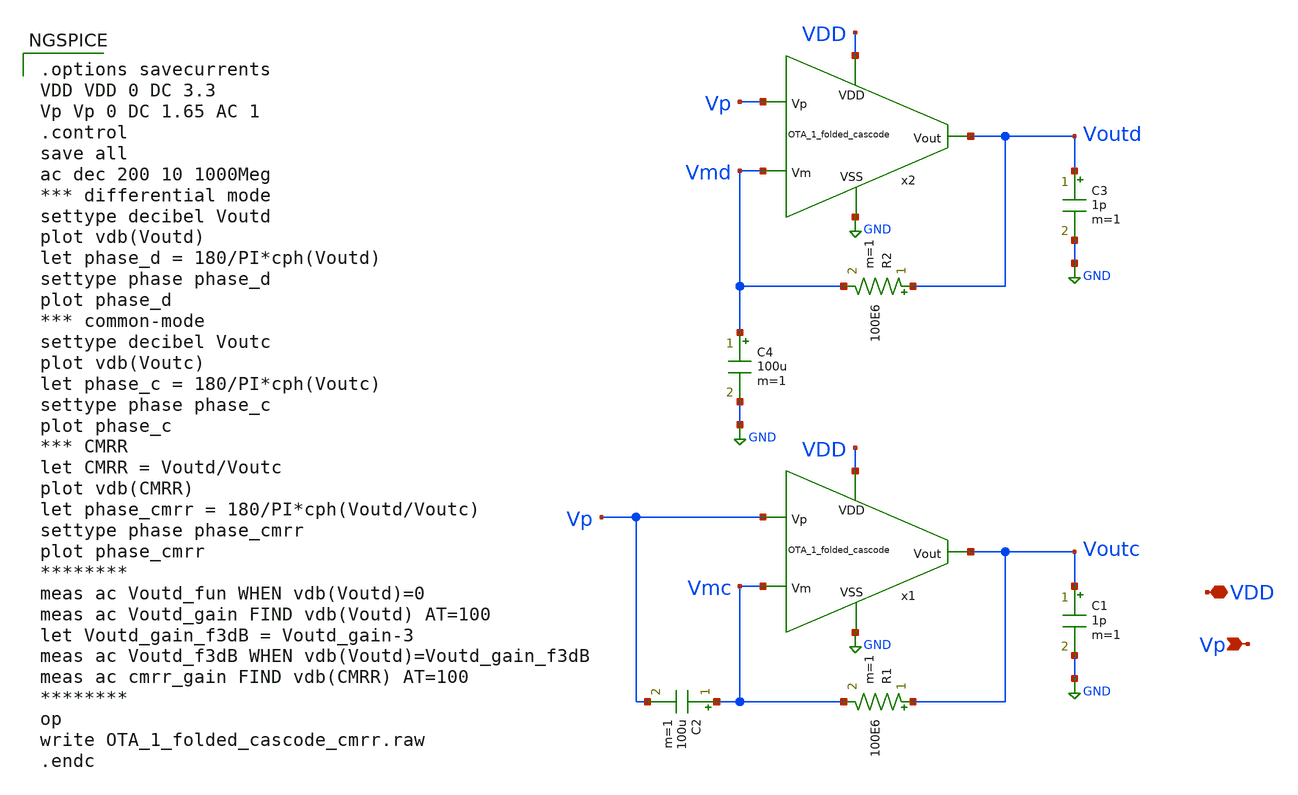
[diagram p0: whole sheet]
** sch_path: xschem/OTA_1_folded_cascode_cmrr.sch
**.subckt OTA_1_folded_cascode_cmrr VDD Vp
*.iopin VDD
*.ipin Vp
C1 Voutc GND 1p m=1
R1 Voutc Vmc 100E6 m=1
C2 Vmc Vp 100u m=1
x1 VDD Vp GND Vmc Voutc OTA_1_folded_cascode
C3 Voutd GND 1p m=1
R2 Voutd Vmd 100E6 m=1
C4 Vmd GND 100u m=1
x2 VDD Vp GND Vmd Voutd OTA_1_folded_cascode
**** begin user architecture code

.options savecurrents
VDD VDD 0 DC 3.3
Vp Vp 0 DC 1.65 AC 1
.control
save all
ac dec 200 10 1000Meg
*** differential mode
settype decibel Voutd
plot vdb(Voutd)
let phase_d = 180/PI*cph(Voutd)
settype phase phase_d
plot phase_d
*** common-mode
settype decibel Voutc
plot vdb(Voutc)
let phase_c = 180/PI*cph(Voutc)
settype phase phase_c
plot phase_c
*** CMRR
let CMRR = Voutd/Voutc
plot vdb(CMRR)
let phase_cmrr = 180/PI*cph(Voutd/Voutc)
settype phase phase_cmrr
plot phase_cmrr
********
meas ac Voutd_fun WHEN vdb(Voutd)=0
meas ac Voutd_gain FIND vdb(Voutd) AT=100
let Voutd_gain_f3dB = Voutd_gain-3
meas ac Voutd_f3dB WHEN vdb(Voutd)=Voutd_gain_f3dB
meas ac cmrr_gain FIND vdb(CMRR) AT=100
********
op
write OTA_1_folded_cascode_cmrr.raw
.endc



** opencircuitdesign pdks install
.lib $::SKYWATER_MODELS/sky130.lib.spice tt


**** end user architecture code
**.ends

* expanding   symbol:  OTA_1_folded_cascode.sym # of pins=5
** sym_path: xschem/OTA_1_folded_cascode.sym
** sch_path: xschem/OTA_1_folded_cascode.sch
.subckt OTA_1_folded_cascode VDD Vp VSS Vm Vout
*.iopin VDD
*.iopin VSS
*.ipin Vp
*.ipin Vm
*.opin Vout
XM1 Vo1 Vtop VDD VDD sky130_fd_pr__pfet_g5v0d10v5 L=1 W=5 nf=1 ad='int((nf+1)/2) * W/nf * 0.29' as='int((nf+2)/2) * W/nf * 0.29'
+ pd='2*int((nf+1)/2) * (W/nf + 0.29)' ps='2*int((nf+2)/2) * (W/nf + 0.29)' nrd='0.29 / W' nrs='0.29 / W'
+ sa=0 sb=0 sd=0 mult=5 m=5
XM7 Vo1 Vp net1 VSS sky130_fd_pr__nfet_g5v0d10v5 L=1 W=5 nf=1 ad='int((nf+1)/2) * W/nf * 0.29' as='int((nf+2)/2) * W/nf * 0.29'
+ pd='2*int((nf+1)/2) * (W/nf + 0.29)' ps='2*int((nf+2)/2) * (W/nf + 0.29)' nrd='0.29 / W' nrs='0.29 / W'
+ sa=0 sb=0 sd=0 mult=5 m=5
XM2 Vo1 Vtop VDD VDD sky130_fd_pr__pfet_g5v0d10v5 L=1 W=5 nf=1 ad='int((nf+1)/2) * W/nf * 0.29' as='int((nf+2)/2) * W/nf * 0.29'
+ pd='2*int((nf+1)/2) * (W/nf + 0.29)' ps='2*int((nf+2)/2) * (W/nf + 0.29)' nrd='0.29 / W' nrs='0.29 / W'
+ sa=0 sb=0 sd=0 mult=5 m=5
XM3 Vo2 Vtop VDD VDD sky130_fd_pr__pfet_g5v0d10v5 L=1 W=5 nf=1 ad='int((nf+1)/2) * W/nf * 0.29' as='int((nf+2)/2) * W/nf * 0.29'
+ pd='2*int((nf+1)/2) * (W/nf + 0.29)' ps='2*int((nf+2)/2) * (W/nf + 0.29)' nrd='0.29 / W' nrs='0.29 / W'
+ sa=0 sb=0 sd=0 mult=5 m=5
XM4 Vo2 Vtop VDD VDD sky130_fd_pr__pfet_g5v0d10v5 L=1 W=5 nf=1 ad='int((nf+1)/2) * W/nf * 0.29' as='int((nf+2)/2) * W/nf * 0.29'
+ pd='2*int((nf+1)/2) * (W/nf + 0.29)' ps='2*int((nf+2)/2) * (W/nf + 0.29)' nrd='0.29 / W' nrs='0.29 / W'
+ sa=0 sb=0 sd=0 mult=5 m=5
XM5 Vtop Vbias2 Vo1 VDD sky130_fd_pr__pfet_g5v0d10v5 L=1 W=5 nf=1 ad='int((nf+1)/2) * W/nf * 0.29' as='int((nf+2)/2) * W/nf * 0.29'
+ pd='2*int((nf+1)/2) * (W/nf + 0.29)' ps='2*int((nf+2)/2) * (W/nf + 0.29)' nrd='0.29 / W' nrs='0.29 / W'
+ sa=0 sb=0 sd=0 mult=5 m=5
XM6 Vout Vbias2 Vo2 VDD sky130_fd_pr__pfet_g5v0d10v5 L=1 W=5 nf=1 ad='int((nf+1)/2) * W/nf * 0.29' as='int((nf+2)/2) * W/nf * 0.29'
+ pd='2*int((nf+1)/2) * (W/nf + 0.29)' ps='2*int((nf+2)/2) * (W/nf + 0.29)' nrd='0.29 / W' nrs='0.29 / W'
+ sa=0 sb=0 sd=0 mult=5 m=5
XM8 Vo2 Vm net1 VSS sky130_fd_pr__nfet_g5v0d10v5 L=1 W=5 nf=1 ad='int((nf+1)/2) * W/nf * 0.29' as='int((nf+2)/2) * W/nf * 0.29'
+ pd='2*int((nf+1)/2) * (W/nf + 0.29)' ps='2*int((nf+2)/2) * (W/nf + 0.29)' nrd='0.29 / W' nrs='0.29 / W'
+ sa=0 sb=0 sd=0 mult=5 m=5
XM9 net1 Vbias3 net2 VSS sky130_fd_pr__nfet_g5v0d10v5 L=1 W=5 nf=1 ad='int((nf+1)/2) * W/nf * 0.29' as='int((nf+2)/2) * W/nf * 0.29'
+ pd='2*int((nf+1)/2) * (W/nf + 0.29)' ps='2*int((nf+2)/2) * (W/nf + 0.29)' nrd='0.29 / W' nrs='0.29 / W'
+ sa=0 sb=0 sd=0 mult=1.05 m=1.05
XM10 net1 Vbias3 net3 VSS sky130_fd_pr__nfet_g5v0d10v5 L=1 W=5 nf=1 ad='int((nf+1)/2) * W/nf * 0.29'
+ as='int((nf+2)/2) * W/nf * 0.29' pd='2*int((nf+1)/2) * (W/nf + 0.29)' ps='2*int((nf+2)/2) * (W/nf + 0.29)'
+ nrd='0.29 / W' nrs='0.29 / W' sa=0 sb=0 sd=0 mult=1.05 m=1.05
XM11 net2 Vbias4 VSS VSS sky130_fd_pr__nfet_g5v0d10v5 L=1 W=5 nf=1 ad='int((nf+1)/2) * W/nf * 0.29' as='int((nf+2)/2) * W/nf * 0.29'
+ pd='2*int((nf+1)/2) * (W/nf + 0.29)' ps='2*int((nf+2)/2) * (W/nf + 0.29)' nrd='0.29 / W' nrs='0.29 / W'
+ sa=0 sb=0 sd=0 mult=1.05 m=1.05
XM12 net3 Vbias4 VSS VSS sky130_fd_pr__nfet_g5v0d10v5 L=1 W=5 nf=1 ad='int((nf+1)/2) * W/nf * 0.29' as='int((nf+2)/2) * W/nf * 0.29'
+ pd='2*int((nf+1)/2) * (W/nf + 0.29)' ps='2*int((nf+2)/2) * (W/nf + 0.29)' nrd='0.29 / W' nrs='0.29 / W'
+ sa=0 sb=0 sd=0 mult=1.05 m=1.05
XM13 Vtop Vbias3 net4 VSS sky130_fd_pr__nfet_g5v0d10v5 L=1 W=5 nf=1 ad='int((nf+1)/2) * W/nf * 0.29'
+ as='int((nf+2)/2) * W/nf * 0.29' pd='2*int((nf+1)/2) * (W/nf + 0.29)' ps='2*int((nf+2)/2) * (W/nf + 0.29)'
+ nrd='0.29 / W' nrs='0.29 / W' sa=0 sb=0 sd=0 mult=1 m=1
XM14 Vout Vbias3 net5 VSS sky130_fd_pr__nfet_g5v0d10v5 L=1 W=5 nf=1 ad='int((nf+1)/2) * W/nf * 0.29'
+ as='int((nf+2)/2) * W/nf * 0.29' pd='2*int((nf+1)/2) * (W/nf + 0.29)' ps='2*int((nf+2)/2) * (W/nf + 0.29)'
+ nrd='0.29 / W' nrs='0.29 / W' sa=0 sb=0 sd=0 mult=1 m=1
XM15 net4 Vbias4 VSS VSS sky130_fd_pr__nfet_g5v0d10v5 L=1 W=5 nf=1 ad='int((nf+1)/2) * W/nf * 0.29' as='int((nf+2)/2) * W/nf * 0.29'
+ pd='2*int((nf+1)/2) * (W/nf + 0.29)' ps='2*int((nf+2)/2) * (W/nf + 0.29)' nrd='0.29 / W' nrs='0.29 / W'
+ sa=0 sb=0 sd=0 mult=1 m=1
XM16 net5 Vbias4 VSS VSS sky130_fd_pr__nfet_g5v0d10v5 L=1 W=5 nf=1 ad='int((nf+1)/2) * W/nf * 0.29' as='int((nf+2)/2) * W/nf * 0.29'
+ pd='2*int((nf+1)/2) * (W/nf + 0.29)' ps='2*int((nf+2)/2) * (W/nf + 0.29)' nrd='0.29 / W' nrs='0.29 / W'
+ sa=0 sb=0 sd=0 mult=1 m=1
x1 Vbiasp Vbiasn VSS Vbias1 Vbias2 Vbias3 Vbias4 Vlow Vhigh Vncas Vpcas VDD bias_circuit
.ends


* expanding   symbol:  bias_circuit.sym # of pins=12
** sym_path: xschem/bias_circuit.sym
** sch_path: xschem/bias_circuit.sch
.subckt bias_circuit Vbiasp Vbiasn VSS Vbias1 Vbias2 Vbias3 Vbias4 Vlow Vhigh Vncas Vpcas VDD
*.iopin VDD
*.opin Vbiasp
*.opin Vbiasn
*.iopin VSS
*.opin Vbias1
*.opin Vbias2
*.opin Vbias3
*.opin Vbias4
*.opin Vlow
*.opin Vhigh
*.opin Vncas
*.opin Vpcas
XM1 Vbias3 Vbiasp VDD VDD sky130_fd_pr__pfet_g5v0d10v5 L=1 W=5 nf=1 ad='int((nf+1)/2) * W/nf * 0.29'
+ as='int((nf+2)/2) * W/nf * 0.29' pd='2*int((nf+1)/2) * (W/nf + 0.29)' ps='2*int((nf+2)/2) * (W/nf + 0.29)'
+ nrd='0.29 / W' nrs='0.29 / W' sa=0 sb=0 sd=0 mult=5 m=5
XM3w Vbias3 Vbias3 VSS VSS sky130_fd_pr__nfet_g5v0d10v5 L=5 W=5 nf=1 ad='int((nf+1)/2) * W/nf * 0.29'
+ as='int((nf+2)/2) * W/nf * 0.29' pd='2*int((nf+1)/2) * (W/nf + 0.29)' ps='2*int((nf+2)/2) * (W/nf + 0.29)'
+ nrd='0.29 / W' nrs='0.29 / W' sa=0 sb=0 sd=0 mult=2 m=2
XM2 Vbias4 Vbiasp VDD VDD sky130_fd_pr__pfet_g5v0d10v5 L=1 W=5 nf=1 ad='int((nf+1)/2) * W/nf * 0.29'
+ as='int((nf+2)/2) * W/nf * 0.29' pd='2*int((nf+1)/2) * (W/nf + 0.29)' ps='2*int((nf+2)/2) * (W/nf + 0.29)'
+ nrd='0.29 / W' nrs='0.29 / W' sa=0 sb=0 sd=0 mult=5 m=5
XM3 Vbias4 Vbias3 Vlow VSS sky130_fd_pr__nfet_g5v0d10v5 L=1 W=5 nf=1 ad='int((nf+1)/2) * W/nf * 0.29'
+ as='int((nf+2)/2) * W/nf * 0.29' pd='2*int((nf+1)/2) * (W/nf + 0.29)' ps='2*int((nf+2)/2) * (W/nf + 0.29)'
+ nrd='0.29 / W' nrs='0.29 / W' sa=0 sb=0 sd=0 mult=1 m=1
XM4 Vlow Vbias4 VSS VSS sky130_fd_pr__nfet_g5v0d10v5 L=1 W=5 nf=1 ad='int((nf+1)/2) * W/nf * 0.29' as='int((nf+2)/2) * W/nf * 0.29'
+ pd='2*int((nf+1)/2) * (W/nf + 0.29)' ps='2*int((nf+2)/2) * (W/nf + 0.29)' nrd='0.29 / W' nrs='0.29 / W'
+ sa=0 sb=0 sd=0 mult=1 m=1
XM6 net1 Vbias2 net2 VDD sky130_fd_pr__pfet_g5v0d10v5 L=1 W=5 nf=1 ad='int((nf+1)/2) * W/nf * 0.29' as='int((nf+2)/2) * W/nf * 0.29'
+ pd='2*int((nf+1)/2) * (W/nf + 0.29)' ps='2*int((nf+2)/2) * (W/nf + 0.29)' nrd='0.29 / W' nrs='0.29 / W'
+ sa=0 sb=0 sd=0 mult=5 m=5
XM7 Vpcas Vpcas net1 VDD sky130_fd_pr__pfet_g5v0d10v5 L=1 W=5 nf=1 ad='int((nf+1)/2) * W/nf * 0.29' as='int((nf+2)/2) * W/nf * 0.29'
+ pd='2*int((nf+1)/2) * (W/nf + 0.29)' ps='2*int((nf+2)/2) * (W/nf + 0.29)' nrd='0.29 / W' nrs='0.29 / W'
+ sa=0 sb=0 sd=0 mult=5 m=5
XM5 net2 net1 VDD VDD sky130_fd_pr__pfet_g5v0d10v5 L=1 W=5 nf=1 ad='int((nf+1)/2) * W/nf * 0.29' as='int((nf+2)/2) * W/nf * 0.29'
+ pd='2*int((nf+1)/2) * (W/nf + 0.29)' ps='2*int((nf+2)/2) * (W/nf + 0.29)' nrd='0.29 / W' nrs='0.29 / W'
+ sa=0 sb=0 sd=0 mult=5 m=5
XM8 Vpcas Vbias3 net3 VSS sky130_fd_pr__nfet_g5v0d10v5 L=1 W=5 nf=1 ad='int((nf+1)/2) * W/nf * 0.29'
+ as='int((nf+2)/2) * W/nf * 0.29' pd='2*int((nf+1)/2) * (W/nf + 0.29)' ps='2*int((nf+2)/2) * (W/nf + 0.29)'
+ nrd='0.29 / W' nrs='0.29 / W' sa=0 sb=0 sd=0 mult=1 m=1
XM9 net3 Vbias4 VSS VSS sky130_fd_pr__nfet_g5v0d10v5 L=1 W=5 nf=1 ad='int((nf+1)/2) * W/nf * 0.29' as='int((nf+2)/2) * W/nf * 0.29'
+ pd='2*int((nf+1)/2) * (W/nf + 0.29)' ps='2*int((nf+2)/2) * (W/nf + 0.29)' nrd='0.29 / W' nrs='0.29 / W'
+ sa=0 sb=0 sd=0 mult=1 m=1
XM10 Vbias2 Vbias3 net4 VSS sky130_fd_pr__nfet_g5v0d10v5 L=1 W=5 nf=1 ad='int((nf+1)/2) * W/nf * 0.29'
+ as='int((nf+2)/2) * W/nf * 0.29' pd='2*int((nf+1)/2) * (W/nf + 0.29)' ps='2*int((nf+2)/2) * (W/nf + 0.29)'
+ nrd='0.29 / W' nrs='0.29 / W' sa=0 sb=0 sd=0 mult=1 m=1
XM11 net4 Vbias4 VSS VSS sky130_fd_pr__nfet_g5v0d10v5 L=1 W=5 nf=1 ad='int((nf+1)/2) * W/nf * 0.29' as='int((nf+2)/2) * W/nf * 0.29'
+ pd='2*int((nf+1)/2) * (W/nf + 0.29)' ps='2*int((nf+2)/2) * (W/nf + 0.29)' nrd='0.29 / W' nrs='0.29 / W'
+ sa=0 sb=0 sd=0 mult=1 m=1
XM12w Vbias2 Vbias2 VDD VDD sky130_fd_pr__pfet_g5v0d10v5 L=5 W=5 nf=1 ad='int((nf+1)/2) * W/nf * 0.29'
+ as='int((nf+2)/2) * W/nf * 0.29' pd='2*int((nf+1)/2) * (W/nf + 0.29)' ps='2*int((nf+2)/2) * (W/nf + 0.29)'
+ nrd='0.29 / W' nrs='0.29 / W' sa=0 sb=0 sd=0 mult=5 m=5
XM12 Vbias1 Vbias2 Vhigh VDD sky130_fd_pr__pfet_g5v0d10v5 L=1 W=5 nf=1 ad='int((nf+1)/2) * W/nf * 0.29'
+ as='int((nf+2)/2) * W/nf * 0.29' pd='2*int((nf+1)/2) * (W/nf + 0.29)' ps='2*int((nf+2)/2) * (W/nf + 0.29)'
+ nrd='0.29 / W' nrs='0.29 / W' sa=0 sb=0 sd=0 mult=5 m=5
XM13 Vhigh Vbias1 VDD VDD sky130_fd_pr__pfet_g5v0d10v5 L=1 W=5 nf=1 ad='int((nf+1)/2) * W/nf * 0.29'
+ as='int((nf+2)/2) * W/nf * 0.29' pd='2*int((nf+1)/2) * (W/nf + 0.29)' ps='2*int((nf+2)/2) * (W/nf + 0.29)'
+ nrd='0.29 / W' nrs='0.29 / W' sa=0 sb=0 sd=0 mult=5 m=5
XM14 Vbias1 Vbias3 net5 VSS sky130_fd_pr__nfet_g5v0d10v5 L=1 W=5 nf=1 ad='int((nf+1)/2) * W/nf * 0.29'
+ as='int((nf+2)/2) * W/nf * 0.29' pd='2*int((nf+1)/2) * (W/nf + 0.29)' ps='2*int((nf+2)/2) * (W/nf + 0.29)'
+ nrd='0.29 / W' nrs='0.29 / W' sa=0 sb=0 sd=0 mult=1 m=1
XM15 net5 Vbias4 VSS VSS sky130_fd_pr__nfet_g5v0d10v5 L=1 W=5 nf=1 ad='int((nf+1)/2) * W/nf * 0.29' as='int((nf+2)/2) * W/nf * 0.29'
+ pd='2*int((nf+1)/2) * (W/nf + 0.29)' ps='2*int((nf+2)/2) * (W/nf + 0.29)' nrd='0.29 / W' nrs='0.29 / W'
+ sa=0 sb=0 sd=0 mult=1 m=1
XM16 Vncas Vbias2 net6 VDD sky130_fd_pr__pfet_g5v0d10v5 L=1 W=5 nf=1 ad='int((nf+1)/2) * W/nf * 0.29'
+ as='int((nf+2)/2) * W/nf * 0.29' pd='2*int((nf+1)/2) * (W/nf + 0.29)' ps='2*int((nf+2)/2) * (W/nf + 0.29)'
+ nrd='0.29 / W' nrs='0.29 / W' sa=0 sb=0 sd=0 mult=5 m=5
XM17 net6 Vbias1 VDD VDD sky130_fd_pr__pfet_g5v0d10v5 L=1 W=5 nf=1 ad='int((nf+1)/2) * W/nf * 0.29' as='int((nf+2)/2) * W/nf * 0.29'
+ pd='2*int((nf+1)/2) * (W/nf + 0.29)' ps='2*int((nf+2)/2) * (W/nf + 0.29)' nrd='0.29 / W' nrs='0.29 / W'
+ sa=0 sb=0 sd=0 mult=5 m=5
XM18 Vncas Vncas net7 VSS sky130_fd_pr__nfet_g5v0d10v5 L=1 W=5 nf=1 ad='int((nf+1)/2) * W/nf * 0.29'
+ as='int((nf+2)/2) * W/nf * 0.29' pd='2*int((nf+1)/2) * (W/nf + 0.29)' ps='2*int((nf+2)/2) * (W/nf + 0.29)'
+ nrd='0.29 / W' nrs='0.29 / W' sa=0 sb=0 sd=0 mult=1 m=1
XM19 net7 Vbias3 net8 VSS sky130_fd_pr__nfet_g5v0d10v5 L=1 W=5 nf=1 ad='int((nf+1)/2) * W/nf * 0.29'
+ as='int((nf+2)/2) * W/nf * 0.29' pd='2*int((nf+1)/2) * (W/nf + 0.29)' ps='2*int((nf+2)/2) * (W/nf + 0.29)'
+ nrd='0.29 / W' nrs='0.29 / W' sa=0 sb=0 sd=0 mult=1 m=1
XM20 net8 net7 VSS VSS sky130_fd_pr__nfet_g5v0d10v5 L=1 W=5 nf=1 ad='int((nf+1)/2) * W/nf * 0.29' as='int((nf+2)/2) * W/nf * 0.29'
+ pd='2*int((nf+1)/2) * (W/nf + 0.29)' ps='2*int((nf+2)/2) * (W/nf + 0.29)' nrd='0.29 / W' nrs='0.29 / W'
+ sa=0 sb=0 sd=0 mult=1 m=1
x1 VDD VSS Vbiasp Vbiasn beta_multiplier
.ends


* expanding   symbol:  beta_multiplier.sym # of pins=4
** sym_path: xschem/beta_multiplier.sym
** sch_path: xschem/beta_multiplier.sch
.subckt beta_multiplier VDD VSS Vbiasp Vbiasn
*.iopin VDD
*.opin Vbiasp
*.opin Vbiasn
*.iopin VSS
XM1 net2 Vbiasp VDD VDD sky130_fd_pr__pfet_g5v0d10v5 L=1 W=5 nf=1 ad='int((nf+1)/2) * W/nf * 0.29' as='int((nf+2)/2) * W/nf * 0.29'
+ pd='2*int((nf+1)/2) * (W/nf + 0.29)' ps='2*int((nf+2)/2) * (W/nf + 0.29)' nrd='0.29 / W' nrs='0.29 / W'
+ sa=0 sb=0 sd=0 mult=5 m=5
XM3 Vbiasn Vbiasn VSS VSS sky130_fd_pr__nfet_g5v0d10v5 L=1 W=5 nf=1 ad='int((nf+1)/2) * W/nf * 0.29'
+ as='int((nf+2)/2) * W/nf * 0.29' pd='2*int((nf+1)/2) * (W/nf + 0.29)' ps='2*int((nf+2)/2) * (W/nf + 0.29)'
+ nrd='0.29 / W' nrs='0.29 / W' sa=0 sb=0 sd=0 mult=1 m=1
XM2 net3 Vbiasp VDD VDD sky130_fd_pr__pfet_g5v0d10v5 L=1 W=5 nf=1 ad='int((nf+1)/2) * W/nf * 0.29' as='int((nf+2)/2) * W/nf * 0.29'
+ pd='2*int((nf+1)/2) * (W/nf + 0.29)' ps='2*int((nf+2)/2) * (W/nf + 0.29)' nrd='0.29 / W' nrs='0.29 / W'
+ sa=0 sb=0 sd=0 mult=5 m=5
XM4 Vreg Vreg net1 VSS sky130_fd_pr__nfet_g5v0d10v5 L=1 W=5 nf=1 ad='int((nf+1)/2) * W/nf * 0.29' as='int((nf+2)/2) * W/nf * 0.29'
+ pd='2*int((nf+1)/2) * (W/nf + 0.29)' ps='2*int((nf+2)/2) * (W/nf + 0.29)' nrd='0.29 / W' nrs='0.29 / W'
+ sa=0 sb=0 sd=0 mult=12 m=12
Vref1 net2 Vbiasn 0
Vref2 net3 Vreg 0
XR2 VSS net1 VSS sky130_fd_pr__res_xhigh_po W=0.35 L=0.74 mult=1 m=1
XM5 net4 net4 VDD VDD sky130_fd_pr__pfet_g5v0d10v5 L=1 W=5 nf=1 ad='int((nf+1)/2) * W/nf * 0.29' as='int((nf+2)/2) * W/nf * 0.29'
+ pd='2*int((nf+1)/2) * (W/nf + 0.29)' ps='2*int((nf+2)/2) * (W/nf + 0.29)' nrd='0.29 / W' nrs='0.29 / W'
+ sa=0 sb=0 sd=0 mult=5 m=5
XM6 Vbiasp net4 VDD VDD sky130_fd_pr__pfet_g5v0d10v5 L=1 W=5 nf=1 ad='int((nf+1)/2) * W/nf * 0.29' as='int((nf+2)/2) * W/nf * 0.29'
+ pd='2*int((nf+1)/2) * (W/nf + 0.29)' ps='2*int((nf+2)/2) * (W/nf + 0.29)' nrd='0.29 / W' nrs='0.29 / W'
+ sa=0 sb=0 sd=0 mult=5 m=5
XM7 net4 Vreg VSS VSS sky130_fd_pr__nfet_g5v0d10v5 L=1 W=5 nf=1 ad='int((nf+1)/2) * W/nf * 0.29' as='int((nf+2)/2) * W/nf * 0.29'
+ pd='2*int((nf+1)/2) * (W/nf + 0.29)' ps='2*int((nf+2)/2) * (W/nf + 0.29)' nrd='0.29 / W' nrs='0.29 / W'
+ sa=0 sb=0 sd=0 mult=1 m=1
XM8 Vbiasp Vbiasn VSS VSS sky130_fd_pr__nfet_g5v0d10v5 L=1 W=5 nf=1 ad='int((nf+1)/2) * W/nf * 0.29'
+ as='int((nf+2)/2) * W/nf * 0.29' pd='2*int((nf+1)/2) * (W/nf + 0.29)' ps='2*int((nf+2)/2) * (W/nf + 0.29)'
+ nrd='0.29 / W' nrs='0.29 / W' sa=0 sb=0 sd=0 mult=1 m=1
XM9 net5 net5 VDD VDD sky130_fd_pr__pfet_g5v0d10v5 L=40 W=1 nf=1 ad='int((nf+1)/2) * W/nf * 0.29' as='int((nf+2)/2) * W/nf * 0.29'
+ pd='2*int((nf+1)/2) * (W/nf + 0.29)' ps='2*int((nf+2)/2) * (W/nf + 0.29)' nrd='0.29 / W' nrs='0.29 / W'
+ sa=0 sb=0 sd=0 mult=1 m=1
XM10 net5 Vbiasn VSS VSS sky130_fd_pr__nfet_g5v0d10v5 L=1 W=5 nf=1 ad='int((nf+1)/2) * W/nf * 0.29' as='int((nf+2)/2) * W/nf * 0.29'
+ pd='2*int((nf+1)/2) * (W/nf + 0.29)' ps='2*int((nf+2)/2) * (W/nf + 0.29)' nrd='0.29 / W' nrs='0.29 / W'
+ sa=0 sb=0 sd=0 mult=1 m=1
XM11 Vbiasp net5 Vbiasn VSS sky130_fd_pr__nfet_g5v0d10v5 L=2 W=5 nf=1 ad='int((nf+1)/2) * W/nf * 0.29'
+ as='int((nf+2)/2) * W/nf * 0.29' pd='2*int((nf+1)/2) * (W/nf + 0.29)' ps='2*int((nf+2)/2) * (W/nf + 0.29)'
+ nrd='0.29 / W' nrs='0.29 / W' sa=0 sb=0 sd=0 mult=1 m=1
XM12 VDD Vbiasp VDD VDD sky130_fd_pr__pfet_g5v0d10v5 L=25 W=5 nf=1 ad='int((nf+1)/2) * W/nf * 0.29' as='int((nf+2)/2) * W/nf * 0.29'
+ pd='2*int((nf+1)/2) * (W/nf + 0.29)' ps='2*int((nf+2)/2) * (W/nf + 0.29)' nrd='0.29 / W' nrs='0.29 / W'
+ sa=0 sb=0 sd=0 mult=5 m=5
.ends

.GLOBAL GND
.end
